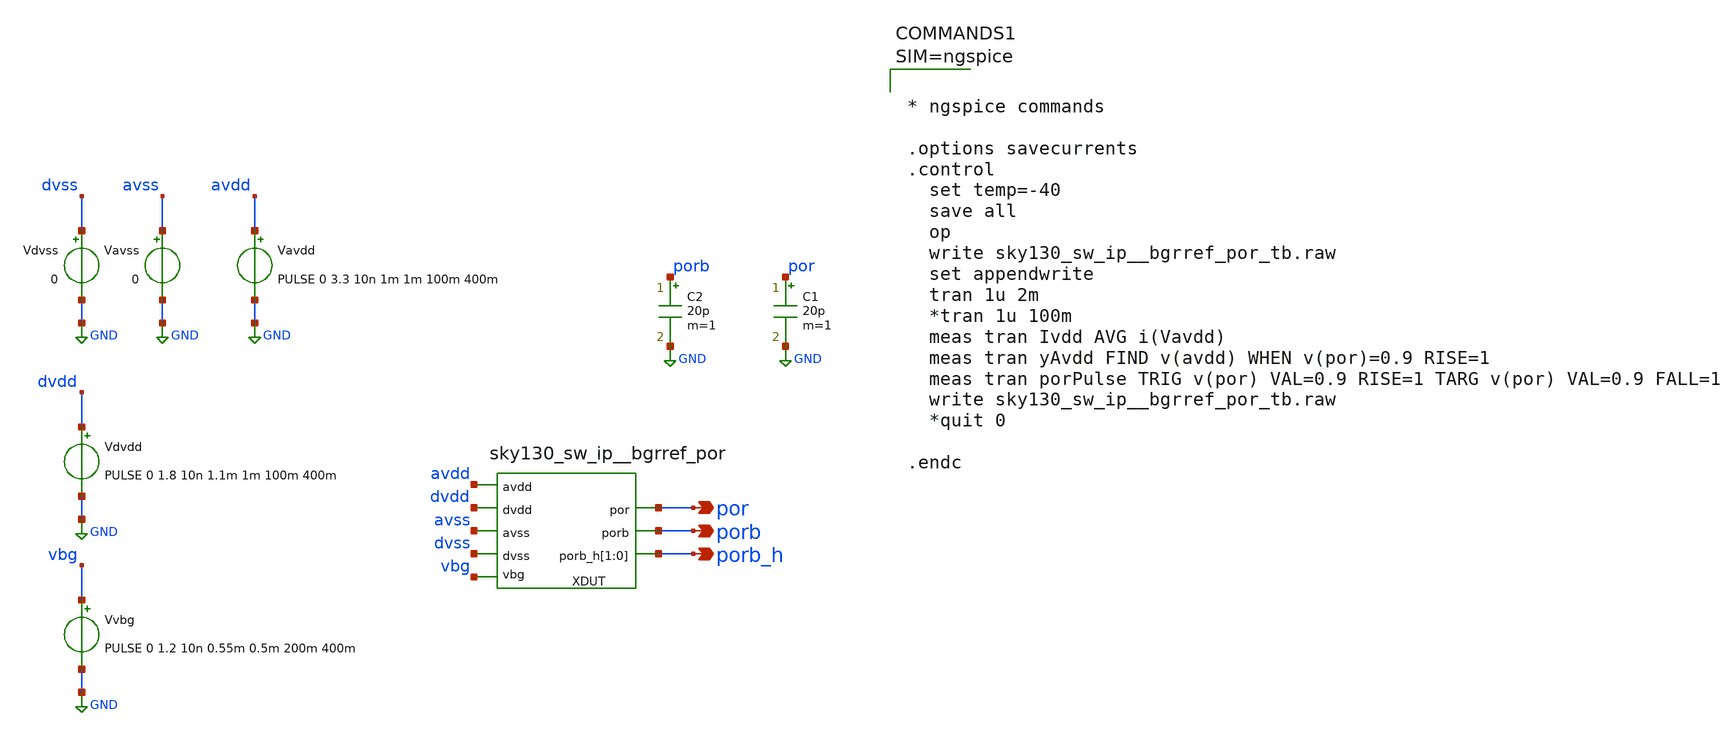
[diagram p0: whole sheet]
** sch_path: xschem_sim/sky130_sw_ip__bgrref_por_tb.sch
**.subckt sky130_sw_ip__bgrref_por_tb por porb porb_h
*.opin por
*.opin porb
*.opin porb_h
Vdvss dvss GND 0
Vavdd avdd GND PULSE 0 3.3 10n 1m 1m 100m 400m
Vavss avss GND 0
Vdvdd dvdd GND PULSE 0 1.8 10n 1.1m 1m 100m 400m
Vvbg vbg GND PULSE 0 1.2 10n 0.55m 0.5m 200m 400m
XDUT vbg por avss avdd dvdd porb dvss porb_h porb_h sky130_sw_ip__bgrref_por
C1 por GND 20p m=1
C2 porb GND 20p m=1
**** begin user architecture code
 .lib $::SKYWATER_MODELS/sky130.lib.spice tt

.include $::SKYWATER_STDCELLS/sky130_fd_sc_hd.spice
.include $::SKYWATER_STDCELLS/../../sky130_fd_sc_hvl/spice/sky130_fd_sc_hvl.spice





* ngspice commands

.options savecurrents
.control
  set temp=-40
  save all
  op
  write sky130_sw_ip__bgrref_por_tb.raw
  set appendwrite
  tran 1u 2m
  *tran 1u 100m
  meas tran Ivdd AVG i(Vavdd)
  meas tran yAvdd FIND v(avdd) WHEN v(por)=0.9 RISE=1
  meas tran porPulse TRIG v(por) VAL=0.9 RISE=1 TARG v(por) VAL=0.9 FALL=1
  write sky130_sw_ip__bgrref_por_tb.raw
  *quit 0

.endc



**** end user architecture code
**.ends
.GLOBAL GND
.end
